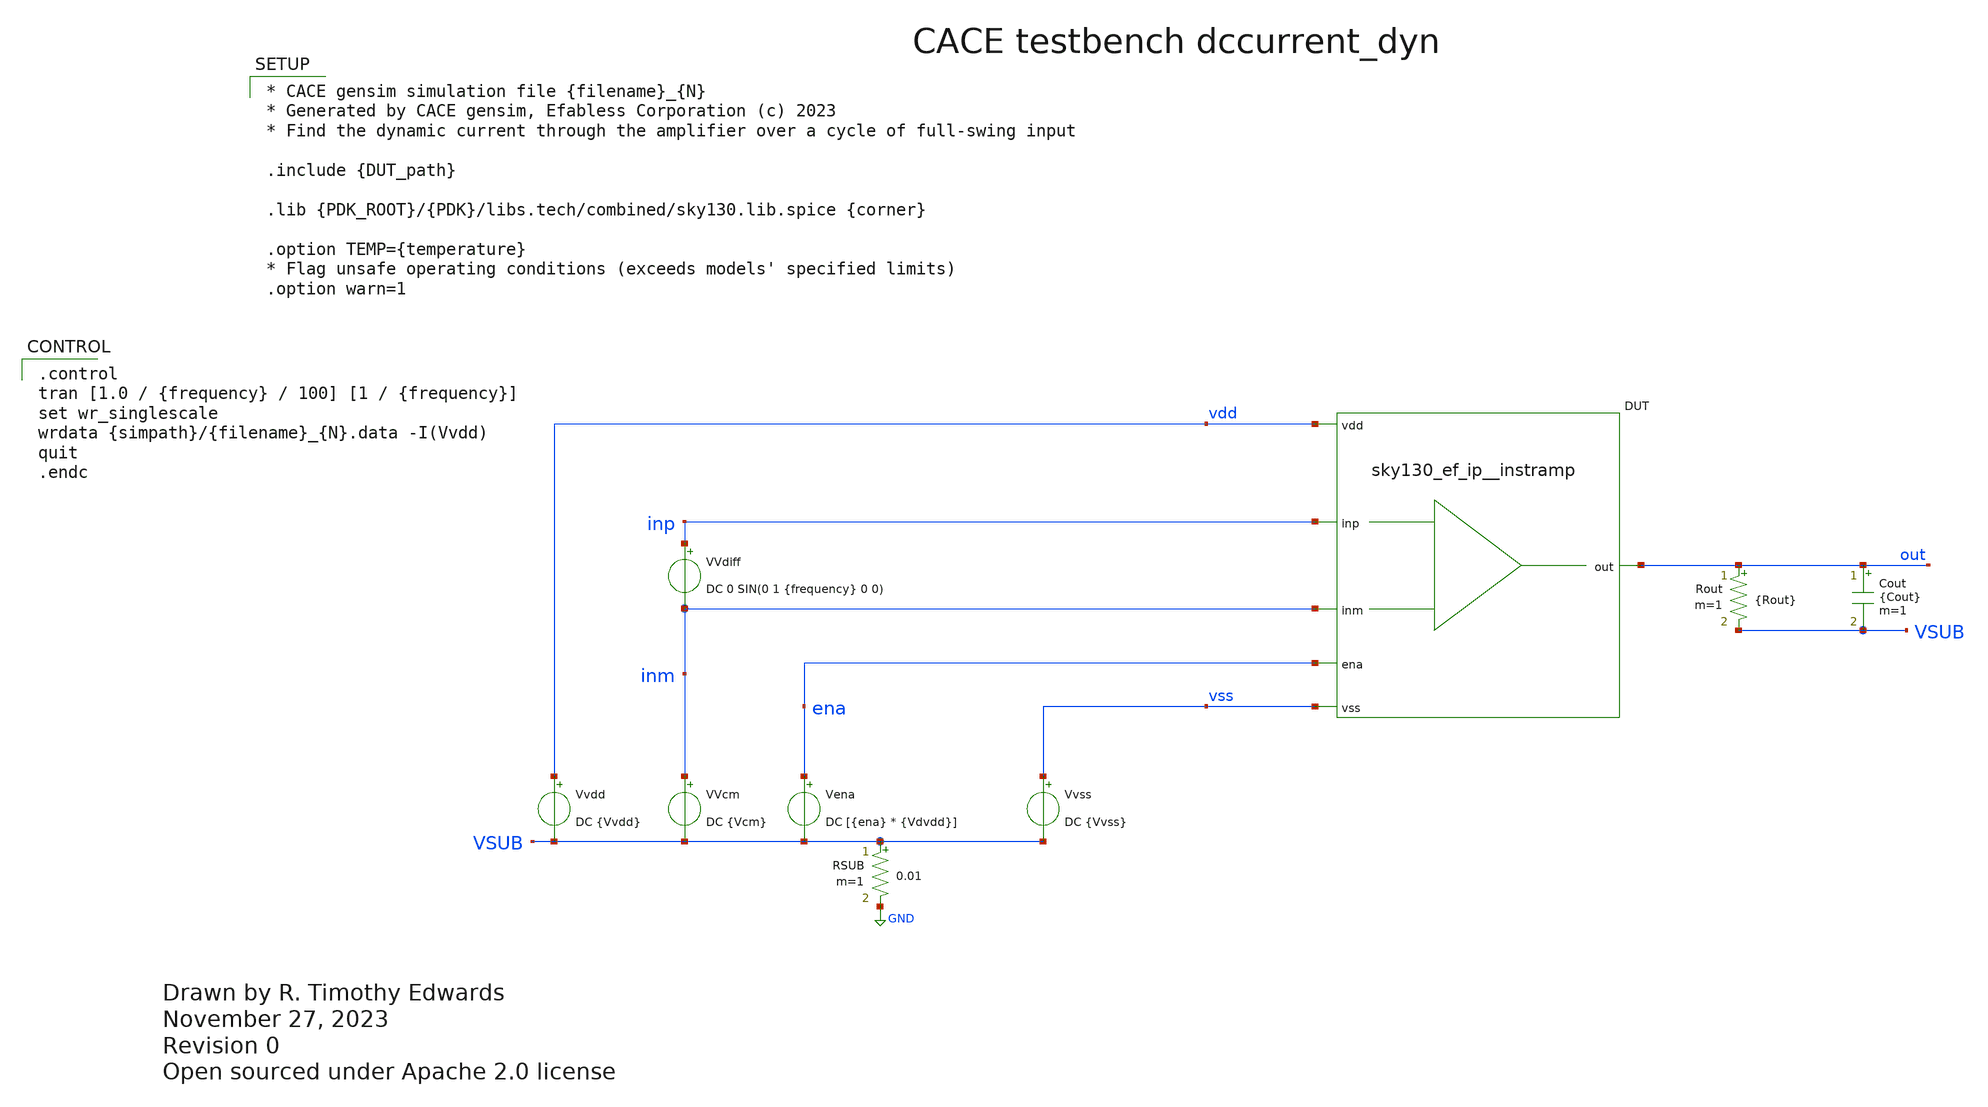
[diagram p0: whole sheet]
** sch_path: cace/dccurrent_dyn.sch
* Open sourced under Apache 2.0 license
**.subckt dccurrent_dyn
VVcm inm VSUB DC {Vcm}
Vena ena VSUB DC [{ena} * {Vdvdd}]
Vvss vss VSUB DC {Vvss}
Rout out VSUB {Rout} m=1
Cout out VSUB {Cout} m=1
Vvdd vdd VSUB DC {Vvdd}
RSUB VSUB GND 0.01 m=1
XDUT {PIN|vdd|vdd} {PIN|vss|vss} {PIN|inm|inm} {PIN|inp|inp} {PIN|out|out} {PIN|ena|ena} {DUT_name}
VVdiff inp inm DC 0 SIN(0 1 {frequency} 0 0)
**** begin user architecture code

.control
tran [1.0 / {frequency} / 100] [1 / {frequency}]
set wr_singlescale
wrdata {simpath}/{filename}_{N}.data -I(Vvdd)
quit
.endc



* CACE gensim simulation file {filename}_{N}
* Generated by CACE gensim, Efabless Corporation (c) 2023
* Find the dynamic current through the amplifier over a cycle of full-swing input

.include {DUT_path}

.lib {PDK_ROOT}/{PDK}/libs.tech/combined/sky130.lib.spice {corner}

.option TEMP={temperature}
* Flag unsafe operating conditions (exceeds models' specified limits)
.option warn=1


**** end user architecture code
**.ends
.GLOBAL GND
.end
